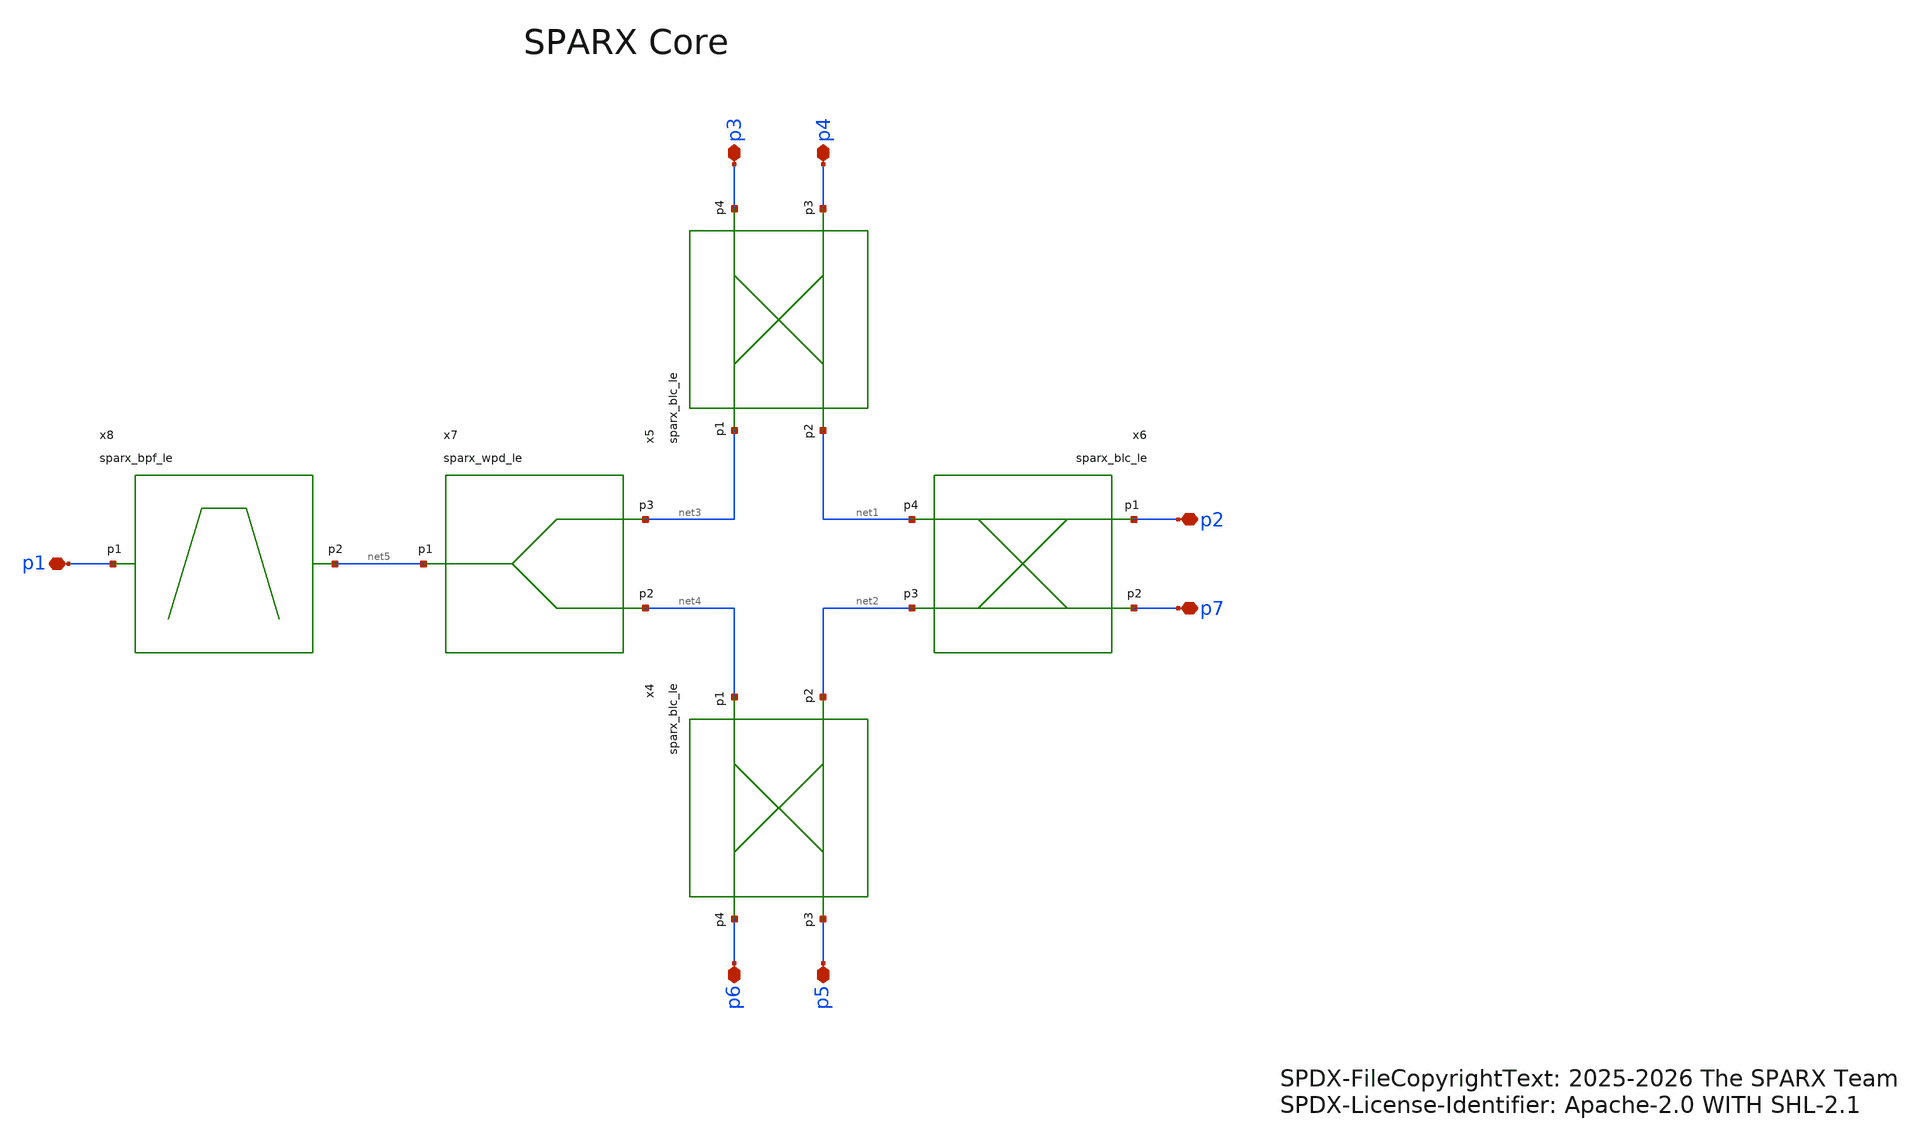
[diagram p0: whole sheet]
** sch_path: schematic/sparx_core.sch
* SPDX-FileCopyrightText: 2025-2026 The SPARX Team
* SPDX-License-Identifier: Apache-2.0 WITH SHL-2.1
**.subckt sparx_core p1 p3 p4 p2 p7 p6 p5
*.iopin p1
*.iopin p3
*.iopin p4
*.iopin p2
*.iopin p7
*.iopin p6
*.iopin p5
x5 net3 net1 p4 p3 sparx_blc_le
x6 p2 p7 net2 net1 sparx_blc_le
x7 net5 net4 net3 sparx_wpd_le
x8 p1 net5 sparx_bpf_le
x4 net4 net2 p5 p6 sparx_blc_le
**.ends
.end
